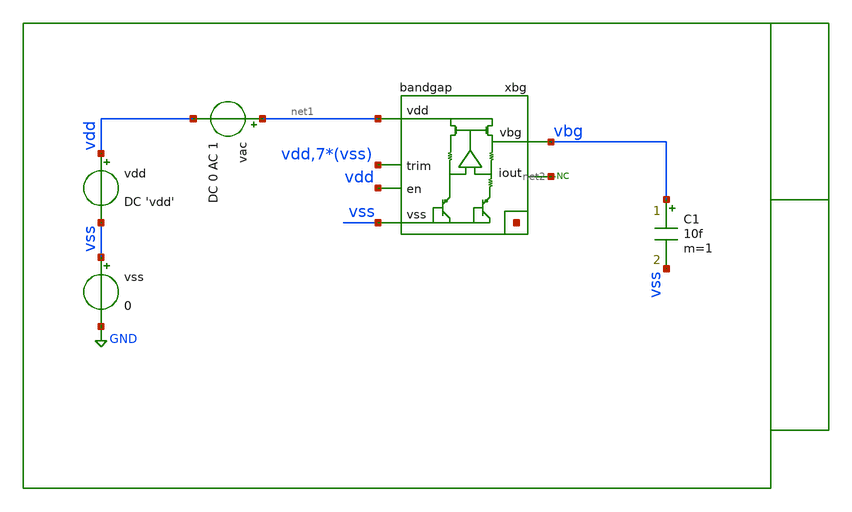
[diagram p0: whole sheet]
** sch_path: xschem/tb/bandgap_cm/bandgap/ac_bandgap_psrr.sch
**.subckt ac_bandgap_psrr
vdd vdd vss DC 'vdd'
vss vss GND 0
* noconn #net2
vac net1 vdd DC 0 AC 1
C1 vbg vss 10f m=1
xbg net1 vbg vss net3[7] net3[6] net3[5] net3[4] net3[3] net3[2] net3[1] net3[0] vdd vss vss vss vss
+ vss vss vss net2 vdd bandgap
**** begin user architecture code

* Control

.param vdd = 3.3
.temp 27

.options reltol = 1e-6

.control

save all
*optran 0 0 0 100n 0.3m 0
ac dec 10 0.01 1e9

let psrr=(1/vbg)
let psrr_db = vdb(psrr)
gnuplot p1 psrr_db

meas ac psrr_dc find psrr_db at=0.01
meas ac psrr_1hz find psrr_db at=1
meas ac psrr_1khz find psrr_db at=1e3
meas ac psrr_10khz find psrr_db at=10e3
meas ac psrr_100khz find psrr_db at=100e3

print psrr_dc
print psrr_1hz
print psrr_1khz
print psrr_10khz
print psrr_100khz

set wr_singlescale
set wr_vecnames
wrdata data.csv psrr psrr_db

.endc
.end


 * Model Corners

.include $::CORNERS/ngspice/tt.spice
*.include $::CORNERS/ngspice/ff.spice
*.include $::CORNERS/ngspice/ss.spice
*.include $::CORNERS/ngspice/sf.spice
*.include $::CORNERS/ngspice/fs.spice

**** end user architecture code
**.ends
.GLOBAL GND
.end
